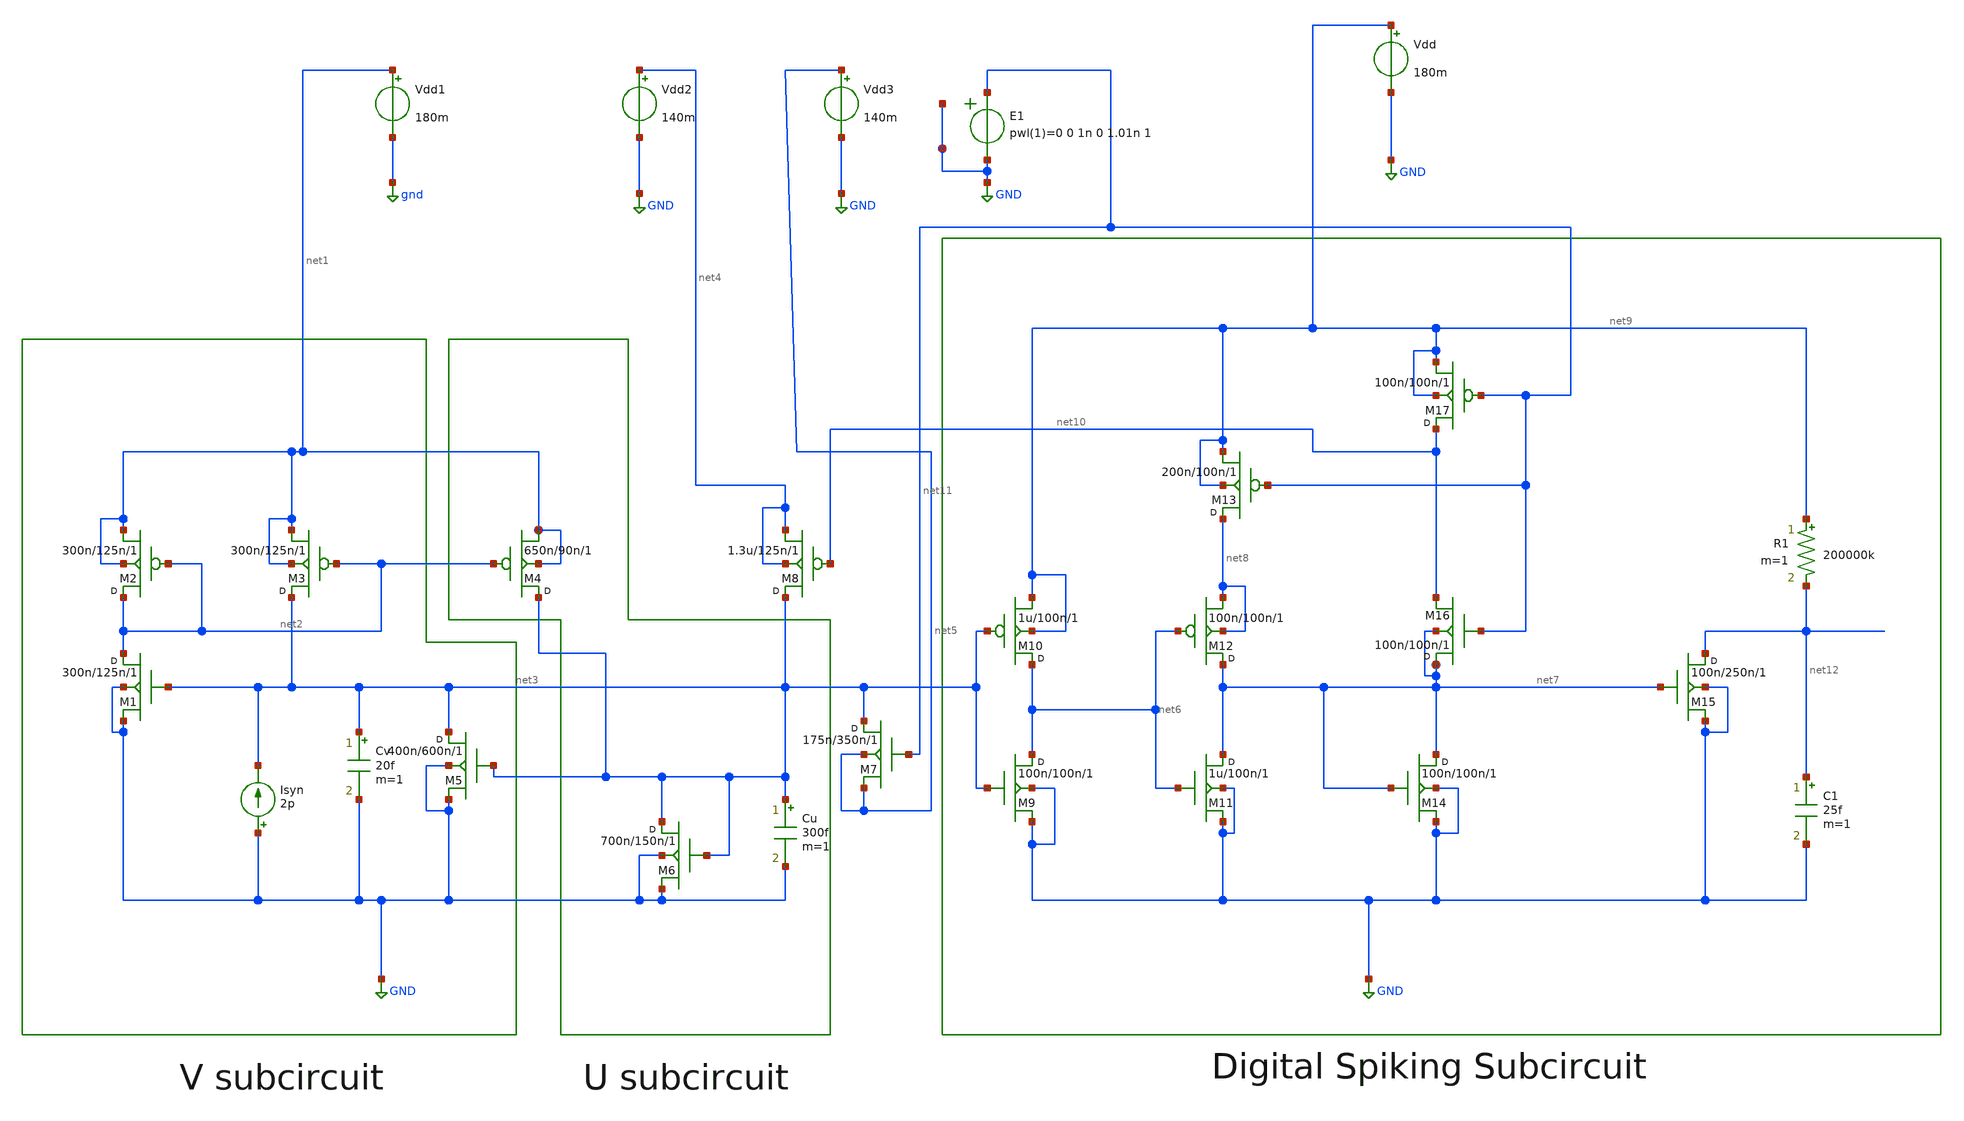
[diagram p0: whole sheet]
** sch_path: SNN.sch
**.subckt SNN
M1 net2 net3 GND GND nmos w=300n l=125n m=1
M2 net2 net2 net1 net1 pmos w=300n l=125n m=1
M3 net3 net2 net1 net1 pmos w=300n l=125n m=1
M4 net3 net2 net1 net1 pmos w=650n l=90n m=1
Isyn GND net3 2p
Cv net3 GND 20f m=1
M5 net3 net3 GND GND nmos w=400n l=600n m=1
M6 net3 net3 GND GND nmos w=700n l=150n m=1
Cu net3 GND 300f m=1
M7 net3 net11 net5 net5 nmos w=175n l=350n m=1
M8 net3 net10 net4 net4 pmos w=1.3u l=125n m=1
M10 net6 net3 net9 net9 pmos w=1u l=100n m=1
M12 net7 net6 net8 net8 pmos w=100n l=100n m=1
M9 net6 net3 GND GND nmos w=100n l=100n m=1
M11 net7 net6 GND GND nmos w=1u l=100n m=1
M13 net8 net11 net9 net9 pmos w=200n l=100n m=1
M17 net10 net11 net9 net9 pmos w=100n l=100n m=1
M16 net7 net11 net10 net7 nmos w=100n l=100n m=1
M14 net7 net7 GND GND nmos w=100n l=100n m=1
M15 net12 net7 GND GND nmos w=100n l=250n m=1
R1 net9 net12 200000k m=1
C1 net12 GND 25f m=1
Vdd net9 GND 180m
Vdd1 net1 gnd 180m
Vdd2 net4 GND 140m
Vdd3 net5 GND 140m
E1 net11 GND pwl(1) GND GND 0 0 1n 0 1.01n 1
**** begin user architecture code

.lib /usr/local/share/pdk/sky130A/libs.tech/ngspice/sky130.lib.spice tt
.tran 1n 10u
.save all
.end

**** end user architecture code
**.ends
.GLOBAL gnd
.GLOBAL GND
.end
